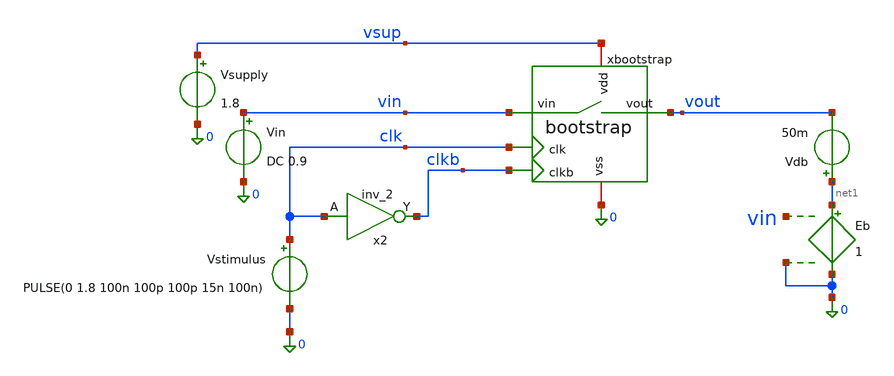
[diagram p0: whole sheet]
** sch_path: xschem/sar-adc_tb/tb2_ron.sch
.lib $::SKYWATER_MODELS/sky130.lib.spice tt
.include $::SKYWATER_STDCELLS/sky130_fd_sc_hd.spice

**.subckt tb2_ron
xbootstrap clk clkb vin vout vsup 0 bootstrap
Vstimulus clk 0 PULSE(0 1.8 100n 100p 100p 15n 100n)
Vsupply vsup 0 1.8
Vin vin 0 DC 0.9
x2 clk 0 0 vsup vsup clkb sky130_fd_sc_hd__inv_2
Eb net1 0 vin 0 1
Vdb net1 vout 50m
**** begin user architecture code


.ic v(vout)=0
.control
 set filetype = ascii
 set wr_vecnames

 echo '' > tb1_track_hold.log
 echo '=== TB1a  boost / settling / droop  vs  vin ======================' >> tb1_track_hold.log
 echo 'boost_err  = 1.8 - max(vgate-vin)  selama track        [target < 50 mV]' >> tb1_track_hold.log
 echo 'ripple     = variasi (vgate-vin) selama track          [target < 10 mV]' >> tb1_track_hold.log
 echo 'vgate_hold = max vgate selama hold                     [target < 50 mV]' >> tb1_track_hold.log
 echo 't_settle   = waktu vout capai 0.5 LSB dari step FS     [target < 15 ns]' >> tb1_track_hold.log
 echo 'err_track  = vin - vout di ujung jendela track         [target < 3.5 mV]' >> tb1_track_hold.log
 echo 'droop      = perubahan vout selama 84 ns hold          [target < 3.5 mV]' >> tb1_track_hold.log
 echo '' >> tb1_track_hold.log

 foreach vsweep 0.1 0.45 0.9 1.35 1.7
  alter Vin dc = $vsweep
  tran 20p 700n
  setplot $curplot

  **Boost Accuracy
  let vboost = v(xbootstrap.vgate) - v(vin)
  meas tran bmin MIN vboost FROM=502n TO=514n
  meas tran bmax MAX vboost FROM=502n TO=514n
  let berr    = (1.8 - bmax)*1e3
  let bripple = (bmax - bmin)*1e3

  **Vgate Hold
  meas tran vgh MAX v(xbootstrap.vgate) FROM=560n TO=595n
  let vgh_mv = vgh*1e3

  ** Settling
  let vtgt = $vsweep - 3.516e-3
  meas tran tset WHEN v(vout)=$&vtgt RISE=1
  let tset_ns = (tset - 100e-9)*1e9
  meas tran vend FIND v(vout) AT=114.9n
  let errtrack = ($vsweep - vend)*1e3

  **Droop
  meas tran vh0 FIND v(vout) AT=514.9n
  meas tran vh1 FIND v(vout) AT=599n
  let droop = (vh1 - vh0)*1e3

  echo 'vin=$vsweep | boost_err=$&berr mV | ripple=$&bripple mV | vgate_hold=$&vgh_mv mV | t_settle=$&tset_ns ns | err_track=$&errtrack mV | droop=$&droop mV'
+ >> tb1_track_hold.log
 end


 echo '' >> tb1_track_hold.log
 echo '=== RELIABILITY (vin = 1.70 V, worst case, siklus 5) ===========' >> tb1_track_hold.log
 echo 'Batas sky130 1.8V device: |V| <= 1.98 V' >> tb1_track_hold.log
 echo '' >> tb1_track_hold.log
 alter Vin dc = 1.70
 tran 20p 700n

 let sw_vgs   = v(xbootstrap.vgate) - v(vin)
 let sw_vgd   = v(xbootstrap.vgate) - v(vout)
 let chtop_v  = v(xbootstrap.ctop)  - v(vsup)
 let drv1_vds = v(xbootstrap.vgate) - v(xbootstrap.net1)
 let drv2_vds = v(xbootstrap.net1)
 let distop_v = v(xbootstrap.vgdistop) - v(xbootstrap.ctop)
 let cboot_v  = v(xbootstrap.ctop) - v(xbootstrap.cbot)

 meas tran m1 MAX  v(xbootstrap.ctop)  FROM=500n TO=600n
 meas tran m2 MAX  v(xbootstrap.vgate) FROM=500n TO=600n
 meas tran m3 MAX  sw_vgs      FROM=500n TO=600n
 meas tran m4 MIN  sw_vgs      FROM=500n TO=600n
 meas tran m5 MAX  sw_vgd      FROM=500n TO=600n
 meas tran m6 MAX  chtop_v     FROM=500n TO=600n
 meas tran m7 MAX  drv1_vds    FROM=500n TO=600n
 meas tran m8 MAX  drv2_vds    FROM=500n TO=600n
 meas tran m9 MIN  distop_v    FROM=500n TO=600n
 meas tran m10 MAX cboot_v     FROM=500n TO=600n

 let m9p = -m9
 echo '  v(ctop) max              = $&m1 V'					>> tb1_track_hold.log
 echo '  v(vgate) max             = $&m2 V'					>> tb1_track_hold.log
 echo '  Mswitch     Vgs max      = $&m3 V     (harus ~1.8 = boost penuh)'	>> tb1_track_hold.log
 echo '  Mswitch     Vgs min      = $&m4 V     (saat hold, = -vin)'		>> tb1_track_hold.log
 echo '  Mswitch     Vgd max      = $&m5 V'					>> tb1_track_hold.log
 echo '  Mchtop      |Vds| max    = $&m6 V     (ctop-vdd)'			>> tb1_track_hold.log
 echo '  Mchtopdrv1  Vds max      = $&m7 V     <-- titik stres tertinggi'	>> tb1_track_hold.log
 echo '  Mchtopdrv2  Vds max      = $&m8 V'					>> tb1_track_hold.log
 echo '  Mdistop     |Vgs| max    = $&m9p V'					>> tb1_track_hold.log
 echo '  Cboot       V max        = $&m10 V'					>> tb1_track_hold.log
 echo ''

 write tb1_track_hold.raw v(vin) v(vout) v(clk) v(clkb) v(xbootstrap.vgate) v(xbootstrap.ctop)
+ v(xbootstrap.cbot) v(xbootstrap.vgdistop) v(xbootstrap.net1)

.endc


**** end user architecture code
**.ends

* expanding   symbol:  bootstrap.sym # of pins=6
** sym_path: xschem/sar-adc/bootstrap.sym
** sch_path: xschem/sar-adc/bootstrap.sch
.subckt bootstrap clk clkb vin vout vdd vss
*.ipin clk
*.ipin clkb
*.ipin vin
*.opin vout
*.iopin vdd
*.iopin vss
XMswitch vin vgate vout vss sky130_fd_pr__nfet_01v8 L=0.15 W=2 nf=1 ad='int((1 + 1)/2) * 2 / 1 * 0.29'
+ as='int((1 + 2)/2) * 2 / 1 * 0.29' pd='2*int((1 + 1)/2) * (2 / 1 + 0.29)' ps='2*int((1 + 2)/2) * (2 / 1 + 0.29)'
+ nrd='0.29 / 2 ' nrs='0.29 / 2 ' sa=0 sb=0 sd=0 mult=1 m=1
XMdisbot cbot vgate vin vss sky130_fd_pr__nfet_01v8 L=0.15 W=1 nf=1 ad='int((1 + 1)/2) * 1 / 1 * 0.29'
+ as='int((1 + 2)/2) * 1 / 1 * 0.29' pd='2*int((1 + 1)/2) * (1 / 1 + 0.29)' ps='2*int((1 + 2)/2) * (1 / 1 + 0.29)'
+ nrd='0.29 / 1 ' nrs='0.29 / 1 ' sa=0 sb=0 sd=0 mult=1 m=1
XCboot ctop cbot sky130_fd_pr__cap_mim_m3_1 W=10 L=10 MF=1 m=1
XMdistop vgate vgdistop ctop ctop sky130_fd_pr__pfet_01v8 L=0.15 W=1 nf=1 ad='int((1 + 1)/2) * 1 / 1 * 0.29'
+ as='int((1 + 2)/2) * 1 / 1 * 0.29' pd='2*int((1 + 1)/2) * (1 / 1 + 0.29)' ps='2*int((1 + 2)/2) * (1 / 1 + 0.29)'
+ nrd='0.29 / 1 ' nrs='0.29 / 1 ' sa=0 sb=0 sd=0 mult=1 m=1
XMchtop ctop vgate vdd ctop sky130_fd_pr__pfet_01v8 L=0.15 W=1 nf=1 ad='int((1 + 1)/2) * 1 / 1 * 0.29'
+ as='int((1 + 2)/2) * 1 / 1 * 0.29' pd='2*int((1 + 1)/2) * (1 / 1 + 0.29)' ps='2*int((1 + 2)/2) * (1 / 1 + 0.29)'
+ nrd='0.29 / 1 ' nrs='0.29 / 1 ' sa=0 sb=0 sd=0 mult=1 m=1
XMdistopdrv vgdistop vgate cbot vss sky130_fd_pr__nfet_01v8 L=0.15 W=0.5 nf=1 ad='int((1 + 1)/2) * 0.5 / 1 * 0.29'
+ as='int((1 + 2)/2) * 0.5 / 1 * 0.29' pd='2*int((1 + 1)/2) * (0.5 / 1 + 0.29)' ps='2*int((1 + 2)/2) * (0.5 / 1 + 0.29)'
+ nrd='0.29 / 0.5 ' nrs='0.29 / 0.5 ' sa=0 sb=0 sd=0 mult=1 m=1
XMchtopdrv2 vschtopdrv1 clkb vss vss sky130_fd_pr__nfet_01v8 L=0.15 W=1 nf=1 ad='int((1 + 1)/2) * 1 / 1 * 0.29'
+ as='int((1 + 2)/2) * 1 / 1 * 0.29' pd='2*int((1 + 1)/2) * (1 / 1 + 0.29)' ps='2*int((1 + 2)/2) * (1 / 1 + 0.29)'
+ nrd='0.29 / 1 ' nrs='0.29 / 1 ' sa=0 sb=0 sd=0 mult=1 m=1
XMchbot cbot clkb vss vss sky130_fd_pr__nfet_01v8 L=0.15 W=1 nf=1 ad='int((1 + 1)/2) * 1 / 1 * 0.29'
+ as='int((1 + 2)/2) * 1 / 1 * 0.29' pd='2*int((1 + 1)/2) * (1 / 1 + 0.29)' ps='2*int((1 + 2)/2) * (1 / 1 + 0.29)'
+ nrd='0.29 / 1 ' nrs='0.29 / 1 ' sa=0 sb=0 sd=0 mult=1 m=1
XM1 vgdistop clk vdd vdd sky130_fd_pr__pfet_01v8 L=0.15 W=1 nf=1 ad='int((1 + 1)/2) * 1 / 1 * 0.29' as='int((1 + 2)/2) * 1 / 1 * 0.29'
+ pd='2*int((1 + 1)/2) * (1 / 1 + 0.29)' ps='2*int((1 + 2)/2) * (1 / 1 + 0.29)' nrd='0.29 / 1 ' nrs='0.29 / 1 '
+ sa=0 sb=0 sd=0 mult=1 m=1
XM2 vgdistop clk cbot vss sky130_fd_pr__nfet_01v8 L=0.15 W=0.5 nf=1 ad='int((1 + 1)/2) * 0.5 / 1 * 0.29'
+ as='int((1 + 2)/2) * 0.5 / 1 * 0.29' pd='2*int((1 + 1)/2) * (0.5 / 1 + 0.29)' ps='2*int((1 + 2)/2) * (0.5 / 1 + 0.29)'
+ nrd='0.29 / 0.5 ' nrs='0.29 / 0.5 ' sa=0 sb=0 sd=0 mult=1 m=1
XXMchtopdrv1 vgate vdd vschtopdrv1 vss sky130_fd_pr__nfet_g5v0d10v5 L=0.5 W=3 nf=1 ad='int((1 + 1)/2) * 3 / 1 * 0.29'
+ as='int((1 + 2)/2) * 3 / 1 * 0.29' pd='2*int((1 + 1)/2) * (3 / 1 + 0.29)' ps='2*int((1 + 2)/2) * (3 / 1 + 0.29)'
+ nrd='0.29 / 3 ' nrs='0.29 / 3 ' sa=0 sb=0 sd=0 mult=1 m=1
.ends

.end
